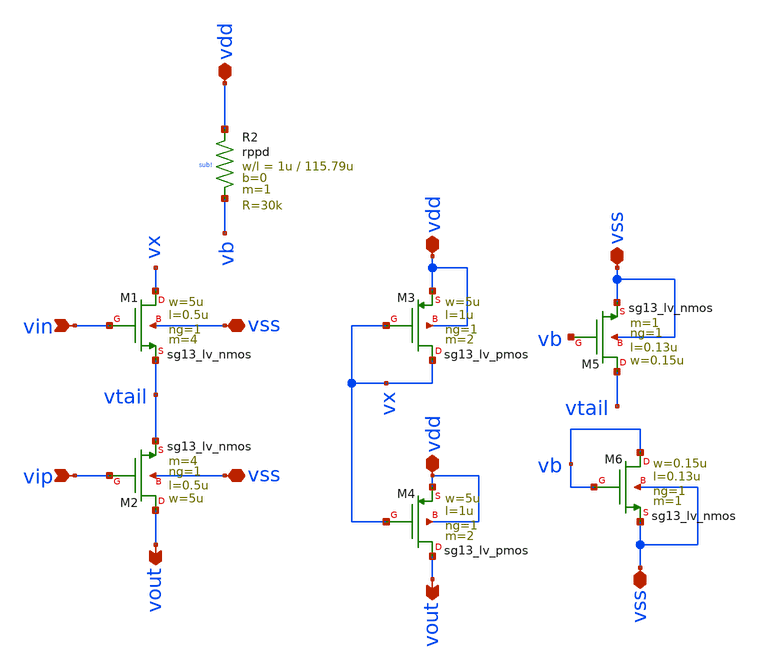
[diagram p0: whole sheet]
** sch_path: macros/heichips26_chronosense/schematic/xschem/ota.sch
**.subckt ota vdd vss vdd vout vout vin vip vdd vss vss vss
*.iopin vdd
*.iopin vss
*.iopin vdd
*.opin vout
*.opin vout
*.ipin vin
*.ipin vip
*.iopin vdd
*.iopin vss
*.iopin vss
*.iopin vss
XM1 vx vin vtail vss sg13_lv_nmos w=5u l=0.5u ng=1 m=4 mm_ok=1
XM3 vx vx vdd vdd sg13_lv_pmos w=5u l=1u ng=1 m=2 mm_ok=1
XM2 vout vip vtail vss sg13_lv_nmos w=5u l=0.5u ng=1 m=4 mm_ok=1
XM6 vb vb vss vss sg13_lv_nmos w=0.15u l=0.13u ng=1 m=1 mm_ok=1
XM5 vtail vb vss vss sg13_lv_nmos w=0.15u l=0.13u ng=1 m=1 mm_ok=1
XM4 vout vx vdd vdd sg13_lv_pmos w=5u l=1u ng=1 m=2 mm_ok=1
XR2 vdd vb sub! rppd w=1u l=115.79u m=1 b=0 mm_ok=1
**.ends
.end
